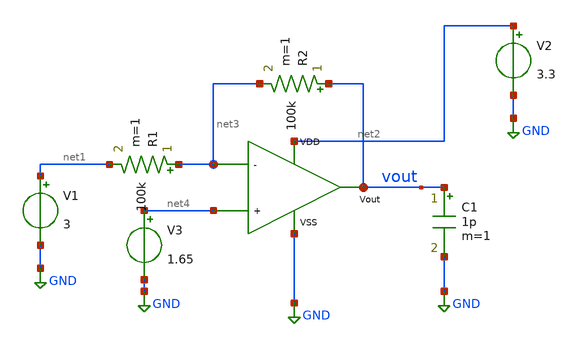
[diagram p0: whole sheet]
** sch_path: xschem/ota_miller/prueba.sch
**.subckt prueba
x1 net2 vout net4 net3 GND ota_n_in
R1 net3 net1 100k m=1
R2 vout net3 100k m=1
V1 net1 GND 3
V2 net2 GND 3.3
C1 vout GND 1p m=1
V3 net4 GND 1.65
**** begin user architecture code


.control
save all
* Coloracion de graficas
set color0=white
set color1=black
set color2=blue
set color3=red
set xbrushwidth=2

* 1. Convertir V1 a onda senoidal: Offset = 1.65V, Amplitud = 0.5V, Frecuencia = 1kHz
alter V1 sin(1.65 0.5 1k)

* 2. Simular 5 ms con paso de 1 us (5 ciclos de 1 kHz)
tran 1u 2m

* 3. Graficar la señal de salida Vout
plot v(Vout) title 'Respuesta Transitoria Inversor OTA 5T' xlabel 'Tiempo (s)' ylabel 'Voltaje (V)'
.endc




.include /home/ringosinye/eda/pdks/gf180mcuD/libs.tech/ngspice/design.ngspice
.lib /home/ringosinye/eda/pdks/gf180mcuD/libs.tech/ngspice/sm141064.ngspice typical
.param sw_stat_mismatch = 0


**** end user architecture code
**.ends

* expanding   symbol:  ota_n_in.sym # of pins=5
** sym_path: xschem/ota_miller/ota_n_in.sym
** sch_path: xschem/ota_miller/ota_n_in.sch
.subckt ota_n_in VDD Vout + - VSS
*.opin Vout
*.ipin VSS
*.ipin VDD
*.ipin +
*.ipin -
I0 VDD net3 10u
XM1 net2 + net1 GND nfet_03v3 L=0.28u W=0.22u nf=1 ad='int((nf+1)/2) * W/nf * 0.18u' as='int((nf+2)/2) * W/nf * 0.18u'
+ pd='2*int((nf+1)/2) * (W/nf + 0.18u)' ps='2*int((nf+2)/2) * (W/nf + 0.18u)' nrd='0.18u / W' nrs='0.18u / W'
+ sa=0 sb=0 sd=0 m=1 par=1
XM2 Vout - net1 GND nfet_03v3 L=0.28u W=0.22u nf=1 ad='int((nf+1)/2) * W/nf * 0.18u' as='int((nf+2)/2) * W/nf * 0.18u'
+ pd='2*int((nf+1)/2) * (W/nf + 0.18u)' ps='2*int((nf+2)/2) * (W/nf + 0.18u)' nrd='0.18u / W' nrs='0.18u / W'
+ sa=0 sb=0 sd=0 m=1 par=1
XM3 net2 net2 VDD VDD pfet_03v3 L=0.28u W=0.22u nf=1 ad='int((nf+1)/2) * W/nf * 0.18u' as='int((nf+2)/2) * W/nf * 0.18u'
+ pd='2*int((nf+1)/2) * (W/nf + 0.18u)' ps='2*int((nf+2)/2) * (W/nf + 0.18u)' nrd='0.18u / W' nrs='0.18u / W'
+ sa=0 sb=0 sd=0 m=1 par=1
XM4 Vout net2 VDD VDD pfet_03v3 L=0.28u W=0.22u nf=1 ad='int((nf+1)/2) * W/nf * 0.18u' as='int((nf+2)/2) * W/nf * 0.18u'
+ pd='2*int((nf+1)/2) * (W/nf + 0.18u)' ps='2*int((nf+2)/2) * (W/nf + 0.18u)' nrd='0.18u / W' nrs='0.18u / W'
+ sa=0 sb=0 sd=0 m=1 par=1
XM5 net1 net3 VSS GND nfet_03v3 L=0.28u W=0.22u nf=1 ad='int((nf+1)/2) * W/nf * 0.18u' as='int((nf+2)/2) * W/nf * 0.18u'
+ pd='2*int((nf+1)/2) * (W/nf + 0.18u)' ps='2*int((nf+2)/2) * (W/nf + 0.18u)' nrd='0.18u / W' nrs='0.18u / W'
+ sa=0 sb=0 sd=0 m=1 par=1
XM6 net3 net3 VSS GND nfet_03v3 L=0.28u W=0.22u nf=1 ad='int((nf+1)/2) * W/nf * 0.18u' as='int((nf+2)/2) * W/nf * 0.18u'
+ pd='2*int((nf+1)/2) * (W/nf + 0.18u)' ps='2*int((nf+2)/2) * (W/nf + 0.18u)' nrd='0.18u / W' nrs='0.18u / W'
+ sa=0 sb=0 sd=0 m=1 par=1
.ends

.GLOBAL GND
.end
